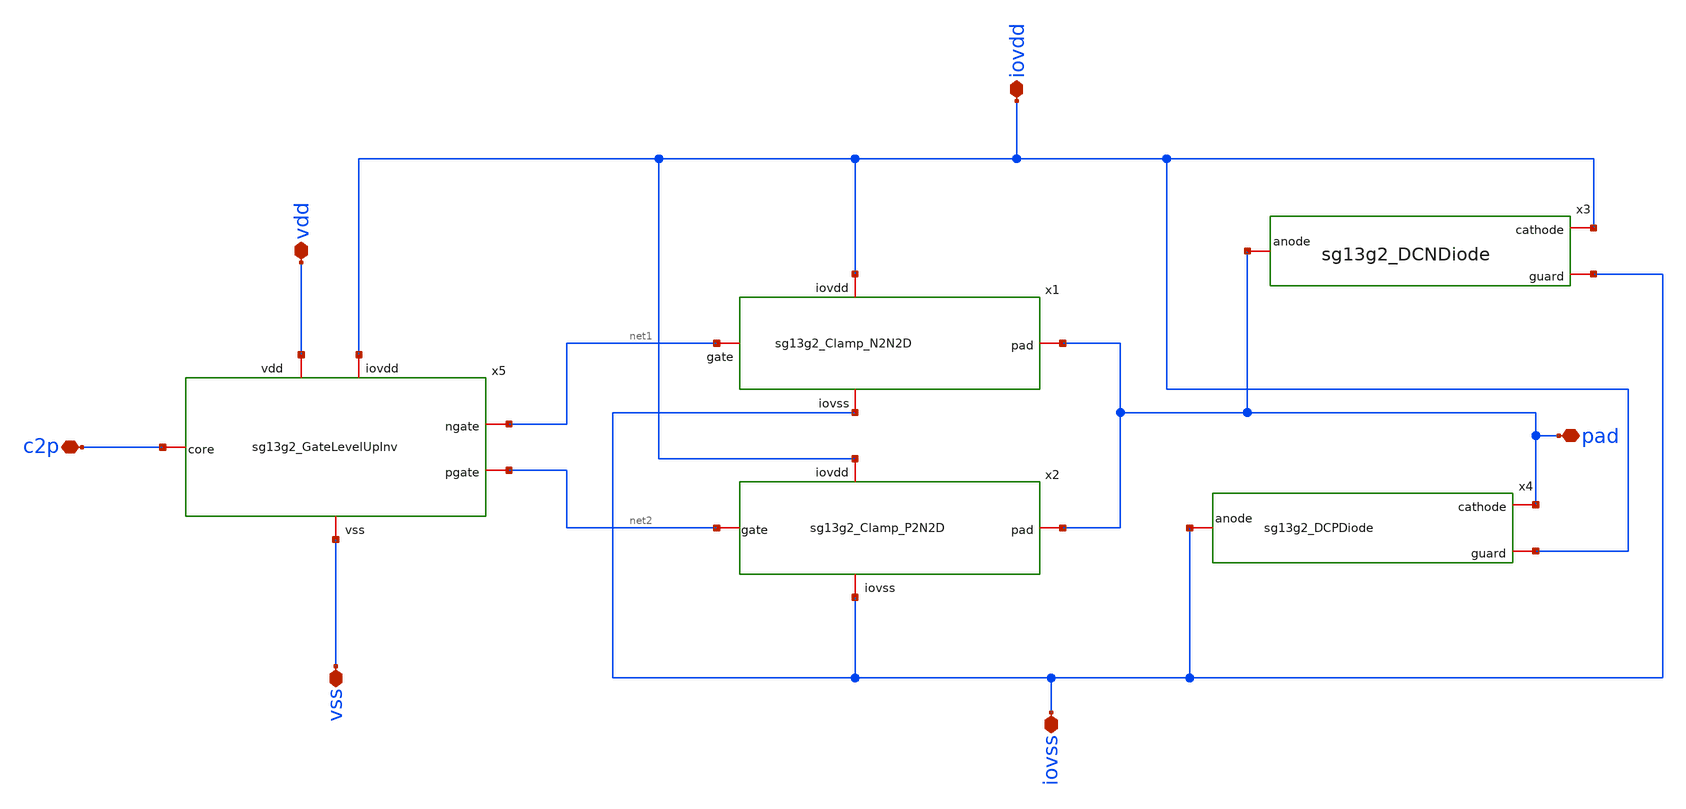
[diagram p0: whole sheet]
** sch_path: ihp-sg13g2/libs.ref/sg13g2_io/xschem/sg13g2_IOPadOut4mA.sch
**.subckt sg13g2_IOPadOut4mA vdd vss iovss iovdd c2p pad
*.iopin vdd
*.iopin vss
*.iopin iovss
*.iopin iovdd
*.iopin c2p
*.iopin pad
x1 iovdd pad net1 iovss sg13g2_Clamp_N2N2D
x2 iovdd net2 iovss pad sg13g2_Clamp_P2N2D
x3 iovdd pad iovss sg13g2_DCNDiode
x4 pad iovss iovdd sg13g2_DCPDiode
x5 vdd iovdd net1 net2 c2p vss sg13g2_GateLevelUpInv
**.ends
.end
